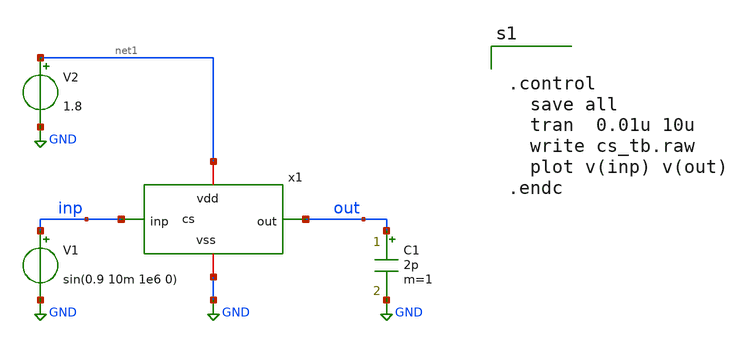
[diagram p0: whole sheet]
** sch_path: xschem/cs_tb.sch
**.subckt cs_tb
x1 out inp net1 GND cs
V1 inp GND sin(0.9 10m 1e6 0)
V2 net1 GND 1.8
C1 out GND 2p m=1
**** begin user architecture code

** opencircuitdesign pdks install
.lib $::SKYWATER_MODELS/sky130.lib.spice tt




.control
  save all
  tran  0.01u 10u
  write cs_tb.raw
  plot v(inp) v(out)
.endc


**** end user architecture code
**.ends

* expanding   symbol:  cs.sym # of pins=4
** sym_path: xschem/cs.sym
.include cs_pex.spice
.GLOBAL GND
.end
